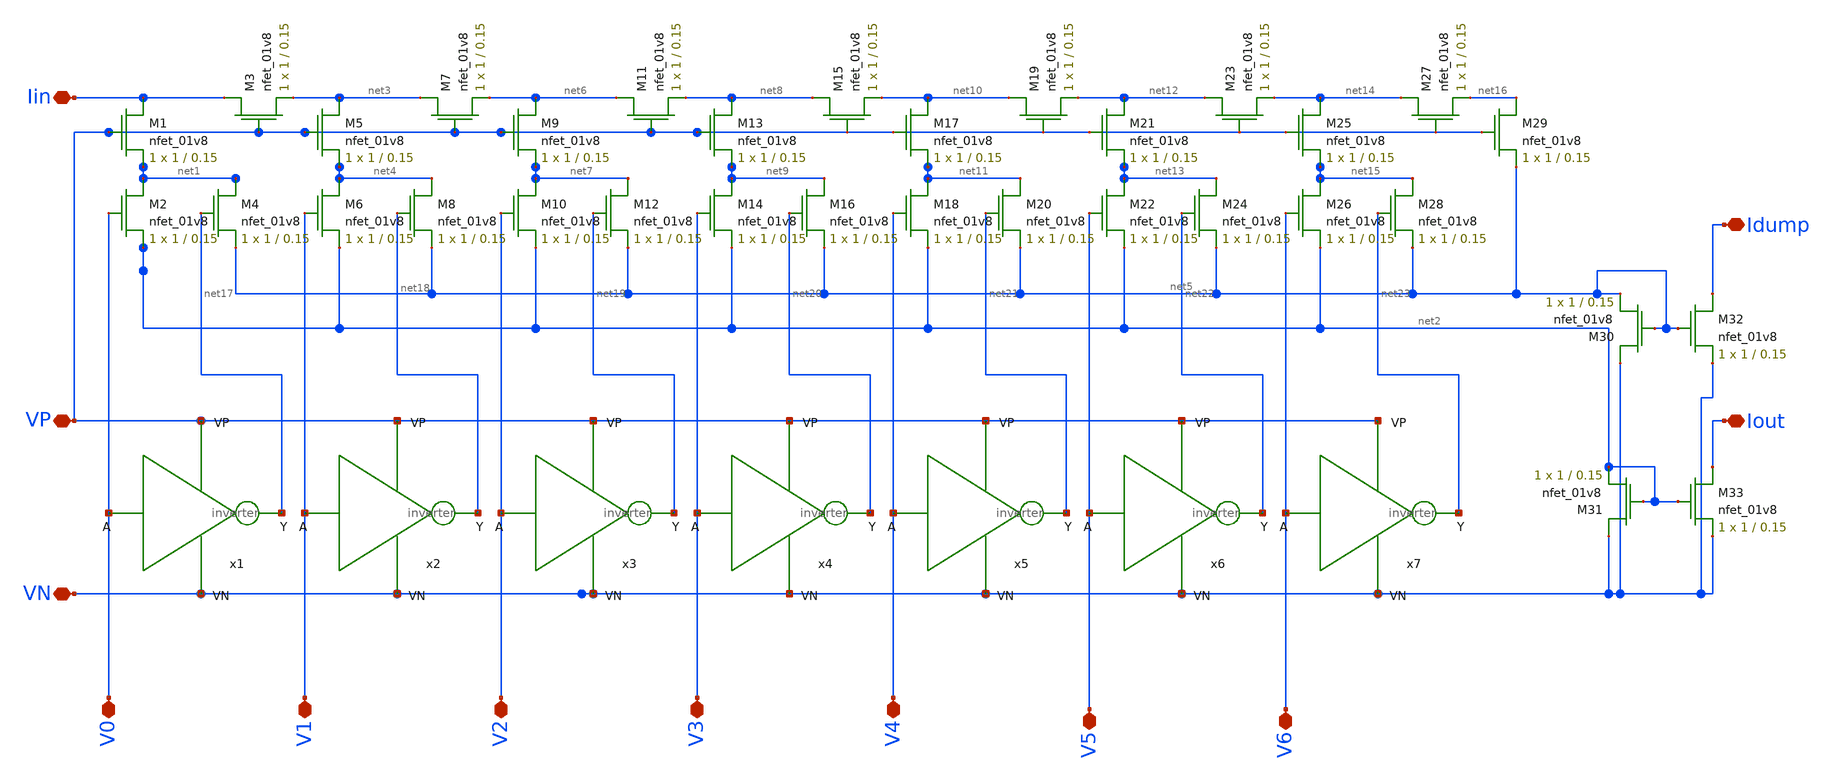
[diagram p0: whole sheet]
** sch_path: ladder.sch
**.subckt ladder VP Iin V0 V1 V2 V3 V4 V5 V6 VN Idump Iout
*.iopin VP
*.iopin Iin
*.iopin V0
*.iopin V1
*.iopin V2
*.iopin V3
*.iopin V4
*.iopin V5
*.iopin V6
*.iopin VN
*.iopin Idump
*.iopin Iout
XM1 Iin VP net1 GND sky130_fd_pr__nfet_01v8 L=0.15 W=1 nf=1 ad='int((nf+1)/2) * W/nf * 0.29' as='int((nf+2)/2) * W/nf * 0.29'
+ pd='2*int((nf+1)/2) * (W/nf + 0.29)' ps='2*int((nf+2)/2) * (W/nf + 0.29)' nrd='0.29 / W' nrs='0.29 / W'
+ sa=0 sb=0 sd=0 mult=1 m=1
XM3 Iin VP net3 GND sky130_fd_pr__nfet_01v8 L=0.15 W=1 nf=1 ad='int((nf+1)/2) * W/nf * 0.29' as='int((nf+2)/2) * W/nf * 0.29'
+ pd='2*int((nf+1)/2) * (W/nf + 0.29)' ps='2*int((nf+2)/2) * (W/nf + 0.29)' nrd='0.29 / W' nrs='0.29 / W'
+ sa=0 sb=0 sd=0 mult=1 m=1
XM5 net3 VP net4 GND sky130_fd_pr__nfet_01v8 L=0.15 W=1 nf=1 ad='int((nf+1)/2) * W/nf * 0.29' as='int((nf+2)/2) * W/nf * 0.29'
+ pd='2*int((nf+1)/2) * (W/nf + 0.29)' ps='2*int((nf+2)/2) * (W/nf + 0.29)' nrd='0.29 / W' nrs='0.29 / W'
+ sa=0 sb=0 sd=0 mult=1 m=1
XM7 net3 VP net6 GND sky130_fd_pr__nfet_01v8 L=0.15 W=1 nf=1 ad='int((nf+1)/2) * W/nf * 0.29' as='int((nf+2)/2) * W/nf * 0.29'
+ pd='2*int((nf+1)/2) * (W/nf + 0.29)' ps='2*int((nf+2)/2) * (W/nf + 0.29)' nrd='0.29 / W' nrs='0.29 / W'
+ sa=0 sb=0 sd=0 mult=1 m=1
XM6 net4 V1 net2 GND sky130_fd_pr__nfet_01v8 L=0.15 W=1 nf=1 ad='int((nf+1)/2) * W/nf * 0.29' as='int((nf+2)/2) * W/nf * 0.29'
+ pd='2*int((nf+1)/2) * (W/nf + 0.29)' ps='2*int((nf+2)/2) * (W/nf + 0.29)' nrd='0.29 / W' nrs='0.29 / W'
+ sa=0 sb=0 sd=0 mult=1 m=1
XM8 net4 net18 net5 GND sky130_fd_pr__nfet_01v8 L=0.15 W=1 nf=1 ad='int((nf+1)/2) * W/nf * 0.29' as='int((nf+2)/2) * W/nf * 0.29'
+ pd='2*int((nf+1)/2) * (W/nf + 0.29)' ps='2*int((nf+2)/2) * (W/nf + 0.29)' nrd='0.29 / W' nrs='0.29 / W'
+ sa=0 sb=0 sd=0 mult=1 m=1
XM2 net1 V0 net2 GND sky130_fd_pr__nfet_01v8 L=0.15 W=1 nf=1 ad='int((nf+1)/2) * W/nf * 0.29' as='int((nf+2)/2) * W/nf * 0.29'
+ pd='2*int((nf+1)/2) * (W/nf + 0.29)' ps='2*int((nf+2)/2) * (W/nf + 0.29)' nrd='0.29 / W' nrs='0.29 / W'
+ sa=0 sb=0 sd=0 mult=1 m=1
XM4 net1 net17 net5 GND sky130_fd_pr__nfet_01v8 L=0.15 W=1 nf=1 ad='int((nf+1)/2) * W/nf * 0.29' as='int((nf+2)/2) * W/nf * 0.29'
+ pd='2*int((nf+1)/2) * (W/nf + 0.29)' ps='2*int((nf+2)/2) * (W/nf + 0.29)' nrd='0.29 / W' nrs='0.29 / W'
+ sa=0 sb=0 sd=0 mult=1 m=1
XM9 net6 VP net7 GND sky130_fd_pr__nfet_01v8 L=0.15 W=1 nf=1 ad='int((nf+1)/2) * W/nf * 0.29' as='int((nf+2)/2) * W/nf * 0.29'
+ pd='2*int((nf+1)/2) * (W/nf + 0.29)' ps='2*int((nf+2)/2) * (W/nf + 0.29)' nrd='0.29 / W' nrs='0.29 / W'
+ sa=0 sb=0 sd=0 mult=1 m=1
XM11 net6 VP net8 GND sky130_fd_pr__nfet_01v8 L=0.15 W=1 nf=1 ad='int((nf+1)/2) * W/nf * 0.29' as='int((nf+2)/2) * W/nf * 0.29'
+ pd='2*int((nf+1)/2) * (W/nf + 0.29)' ps='2*int((nf+2)/2) * (W/nf + 0.29)' nrd='0.29 / W' nrs='0.29 / W'
+ sa=0 sb=0 sd=0 mult=1 m=1
XM10 net7 V2 net2 GND sky130_fd_pr__nfet_01v8 L=0.15 W=1 nf=1 ad='int((nf+1)/2) * W/nf * 0.29' as='int((nf+2)/2) * W/nf * 0.29'
+ pd='2*int((nf+1)/2) * (W/nf + 0.29)' ps='2*int((nf+2)/2) * (W/nf + 0.29)' nrd='0.29 / W' nrs='0.29 / W'
+ sa=0 sb=0 sd=0 mult=1 m=1
XM12 net7 net19 net5 GND sky130_fd_pr__nfet_01v8 L=0.15 W=1 nf=1 ad='int((nf+1)/2) * W/nf * 0.29' as='int((nf+2)/2) * W/nf * 0.29'
+ pd='2*int((nf+1)/2) * (W/nf + 0.29)' ps='2*int((nf+2)/2) * (W/nf + 0.29)' nrd='0.29 / W' nrs='0.29 / W'
+ sa=0 sb=0 sd=0 mult=1 m=1
XM13 net8 VP net9 GND sky130_fd_pr__nfet_01v8 L=0.15 W=1 nf=1 ad='int((nf+1)/2) * W/nf * 0.29' as='int((nf+2)/2) * W/nf * 0.29'
+ pd='2*int((nf+1)/2) * (W/nf + 0.29)' ps='2*int((nf+2)/2) * (W/nf + 0.29)' nrd='0.29 / W' nrs='0.29 / W'
+ sa=0 sb=0 sd=0 mult=1 m=1
XM15 net8 VP net10 GND sky130_fd_pr__nfet_01v8 L=0.15 W=1 nf=1 ad='int((nf+1)/2) * W/nf * 0.29' as='int((nf+2)/2) * W/nf * 0.29'
+ pd='2*int((nf+1)/2) * (W/nf + 0.29)' ps='2*int((nf+2)/2) * (W/nf + 0.29)' nrd='0.29 / W' nrs='0.29 / W'
+ sa=0 sb=0 sd=0 mult=1 m=1
XM14 net9 V3 net2 GND sky130_fd_pr__nfet_01v8 L=0.15 W=1 nf=1 ad='int((nf+1)/2) * W/nf * 0.29' as='int((nf+2)/2) * W/nf * 0.29'
+ pd='2*int((nf+1)/2) * (W/nf + 0.29)' ps='2*int((nf+2)/2) * (W/nf + 0.29)' nrd='0.29 / W' nrs='0.29 / W'
+ sa=0 sb=0 sd=0 mult=1 m=1
XM16 net9 net20 net5 GND sky130_fd_pr__nfet_01v8 L=0.15 W=1 nf=1 ad='int((nf+1)/2) * W/nf * 0.29' as='int((nf+2)/2) * W/nf * 0.29'
+ pd='2*int((nf+1)/2) * (W/nf + 0.29)' ps='2*int((nf+2)/2) * (W/nf + 0.29)' nrd='0.29 / W' nrs='0.29 / W'
+ sa=0 sb=0 sd=0 mult=1 m=1
XM17 net10 VP net11 GND sky130_fd_pr__nfet_01v8 L=0.15 W=1 nf=1 ad='int((nf+1)/2) * W/nf * 0.29' as='int((nf+2)/2) * W/nf * 0.29'
+ pd='2*int((nf+1)/2) * (W/nf + 0.29)' ps='2*int((nf+2)/2) * (W/nf + 0.29)' nrd='0.29 / W' nrs='0.29 / W'
+ sa=0 sb=0 sd=0 mult=1 m=1
XM19 net10 VP net12 GND sky130_fd_pr__nfet_01v8 L=0.15 W=1 nf=1 ad='int((nf+1)/2) * W/nf * 0.29' as='int((nf+2)/2) * W/nf * 0.29'
+ pd='2*int((nf+1)/2) * (W/nf + 0.29)' ps='2*int((nf+2)/2) * (W/nf + 0.29)' nrd='0.29 / W' nrs='0.29 / W'
+ sa=0 sb=0 sd=0 mult=1 m=1
XM18 net11 V4 net2 GND sky130_fd_pr__nfet_01v8 L=0.15 W=1 nf=1 ad='int((nf+1)/2) * W/nf * 0.29' as='int((nf+2)/2) * W/nf * 0.29'
+ pd='2*int((nf+1)/2) * (W/nf + 0.29)' ps='2*int((nf+2)/2) * (W/nf + 0.29)' nrd='0.29 / W' nrs='0.29 / W'
+ sa=0 sb=0 sd=0 mult=1 m=1
XM20 net11 net21 net5 GND sky130_fd_pr__nfet_01v8 L=0.15 W=1 nf=1 ad='int((nf+1)/2) * W/nf * 0.29' as='int((nf+2)/2) * W/nf * 0.29'
+ pd='2*int((nf+1)/2) * (W/nf + 0.29)' ps='2*int((nf+2)/2) * (W/nf + 0.29)' nrd='0.29 / W' nrs='0.29 / W'
+ sa=0 sb=0 sd=0 mult=1 m=1
XM21 net12 VP net13 GND sky130_fd_pr__nfet_01v8 L=0.15 W=1 nf=1 ad='int((nf+1)/2) * W/nf * 0.29' as='int((nf+2)/2) * W/nf * 0.29'
+ pd='2*int((nf+1)/2) * (W/nf + 0.29)' ps='2*int((nf+2)/2) * (W/nf + 0.29)' nrd='0.29 / W' nrs='0.29 / W'
+ sa=0 sb=0 sd=0 mult=1 m=1
XM23 net12 VP net14 GND sky130_fd_pr__nfet_01v8 L=0.15 W=1 nf=1 ad='int((nf+1)/2) * W/nf * 0.29' as='int((nf+2)/2) * W/nf * 0.29'
+ pd='2*int((nf+1)/2) * (W/nf + 0.29)' ps='2*int((nf+2)/2) * (W/nf + 0.29)' nrd='0.29 / W' nrs='0.29 / W'
+ sa=0 sb=0 sd=0 mult=1 m=1
XM22 net13 V5 net2 GND sky130_fd_pr__nfet_01v8 L=0.15 W=1 nf=1 ad='int((nf+1)/2) * W/nf * 0.29' as='int((nf+2)/2) * W/nf * 0.29'
+ pd='2*int((nf+1)/2) * (W/nf + 0.29)' ps='2*int((nf+2)/2) * (W/nf + 0.29)' nrd='0.29 / W' nrs='0.29 / W'
+ sa=0 sb=0 sd=0 mult=1 m=1
XM24 net13 net22 net5 GND sky130_fd_pr__nfet_01v8 L=0.15 W=1 nf=1 ad='int((nf+1)/2) * W/nf * 0.29' as='int((nf+2)/2) * W/nf * 0.29'
+ pd='2*int((nf+1)/2) * (W/nf + 0.29)' ps='2*int((nf+2)/2) * (W/nf + 0.29)' nrd='0.29 / W' nrs='0.29 / W'
+ sa=0 sb=0 sd=0 mult=1 m=1
XM25 net14 VP net15 GND sky130_fd_pr__nfet_01v8 L=0.15 W=1 nf=1 ad='int((nf+1)/2) * W/nf * 0.29' as='int((nf+2)/2) * W/nf * 0.29'
+ pd='2*int((nf+1)/2) * (W/nf + 0.29)' ps='2*int((nf+2)/2) * (W/nf + 0.29)' nrd='0.29 / W' nrs='0.29 / W'
+ sa=0 sb=0 sd=0 mult=1 m=1
XM27 net14 VP net16 GND sky130_fd_pr__nfet_01v8 L=0.15 W=1 nf=1 ad='int((nf+1)/2) * W/nf * 0.29' as='int((nf+2)/2) * W/nf * 0.29'
+ pd='2*int((nf+1)/2) * (W/nf + 0.29)' ps='2*int((nf+2)/2) * (W/nf + 0.29)' nrd='0.29 / W' nrs='0.29 / W'
+ sa=0 sb=0 sd=0 mult=1 m=1
XM26 net15 V6 net2 GND sky130_fd_pr__nfet_01v8 L=0.15 W=1 nf=1 ad='int((nf+1)/2) * W/nf * 0.29' as='int((nf+2)/2) * W/nf * 0.29'
+ pd='2*int((nf+1)/2) * (W/nf + 0.29)' ps='2*int((nf+2)/2) * (W/nf + 0.29)' nrd='0.29 / W' nrs='0.29 / W'
+ sa=0 sb=0 sd=0 mult=1 m=1
XM28 net15 net23 net5 GND sky130_fd_pr__nfet_01v8 L=0.15 W=1 nf=1 ad='int((nf+1)/2) * W/nf * 0.29' as='int((nf+2)/2) * W/nf * 0.29'
+ pd='2*int((nf+1)/2) * (W/nf + 0.29)' ps='2*int((nf+2)/2) * (W/nf + 0.29)' nrd='0.29 / W' nrs='0.29 / W'
+ sa=0 sb=0 sd=0 mult=1 m=1
XM29 net16 VP net5 GND sky130_fd_pr__nfet_01v8 L=0.15 W=1 nf=1 ad='int((nf+1)/2) * W/nf * 0.29' as='int((nf+2)/2) * W/nf * 0.29'
+ pd='2*int((nf+1)/2) * (W/nf + 0.29)' ps='2*int((nf+2)/2) * (W/nf + 0.29)' nrd='0.29 / W' nrs='0.29 / W'
+ sa=0 sb=0 sd=0 mult=1 m=1
x1 net17 V0 VP VN inverter
x2 net18 V1 VP VN inverter
x3 net19 V2 VP VN inverter
x4 net20 V3 VP VN inverter
x5 net21 V4 VP VN inverter
x6 net22 V5 VP VN inverter
x7 net23 V6 VP VN inverter
XM30 VN net5 net5 GND sky130_fd_pr__nfet_01v8 L=0.15 W=1 nf=1 ad='int((nf+1)/2) * W/nf * 0.29' as='int((nf+2)/2) * W/nf * 0.29'
+ pd='2*int((nf+1)/2) * (W/nf + 0.29)' ps='2*int((nf+2)/2) * (W/nf + 0.29)' nrd='0.29 / W' nrs='0.29 / W'
+ sa=0 sb=0 sd=0 mult=1 m=1
XM31 VN net2 net2 GND sky130_fd_pr__nfet_01v8 L=0.15 W=1 nf=1 ad='int((nf+1)/2) * W/nf * 0.29' as='int((nf+2)/2) * W/nf * 0.29'
+ pd='2*int((nf+1)/2) * (W/nf + 0.29)' ps='2*int((nf+2)/2) * (W/nf + 0.29)' nrd='0.29 / W' nrs='0.29 / W'
+ sa=0 sb=0 sd=0 mult=1 m=1
XM32 Idump net5 VN GND sky130_fd_pr__nfet_01v8 L=0.15 W=1 nf=1 ad='int((nf+1)/2) * W/nf * 0.29' as='int((nf+2)/2) * W/nf * 0.29'
+ pd='2*int((nf+1)/2) * (W/nf + 0.29)' ps='2*int((nf+2)/2) * (W/nf + 0.29)' nrd='0.29 / W' nrs='0.29 / W'
+ sa=0 sb=0 sd=0 mult=1 m=1
XM33 Iout net2 VN GND sky130_fd_pr__nfet_01v8 L=0.15 W=1 nf=1 ad='int((nf+1)/2) * W/nf * 0.29' as='int((nf+2)/2) * W/nf * 0.29'
+ pd='2*int((nf+1)/2) * (W/nf + 0.29)' ps='2*int((nf+2)/2) * (W/nf + 0.29)' nrd='0.29 / W' nrs='0.29 / W'
+ sa=0 sb=0 sd=0 mult=1 m=1
**.ends

* expanding   symbol:  /home/madvlsi/Documents/MP1/Schematics/inverter.sym # of pins=4
** sym_path: inverter.sym
** sch_path: inverter.sch
.subckt inverter Y A VP VN
*.ipin A
*.opin Y
*.iopin VP
*.iopin VN
XM1 Y A VP VP sky130_fd_pr__pfet_01v8 L=0.15 W=1 nf=1 ad='int((nf+1)/2) * W/nf * 0.29' as='int((nf+2)/2) * W/nf * 0.29'
+ pd='2*int((nf+1)/2) * (W/nf + 0.29)' ps='2*int((nf+2)/2) * (W/nf + 0.29)' nrd='0.29 / W' nrs='0.29 / W'
+ sa=0 sb=0 sd=0 mult=1 m=1
XM2 Y A VN VN sky130_fd_pr__nfet_01v8 L=0.15 W=1 nf=1 ad='int((nf+1)/2) * W/nf * 0.29' as='int((nf+2)/2) * W/nf * 0.29'
+ pd='2*int((nf+1)/2) * (W/nf + 0.29)' ps='2*int((nf+2)/2) * (W/nf + 0.29)' nrd='0.29 / W' nrs='0.29 / W'
+ sa=0 sb=0 sd=0 mult=1 m=1
.ends

.end
